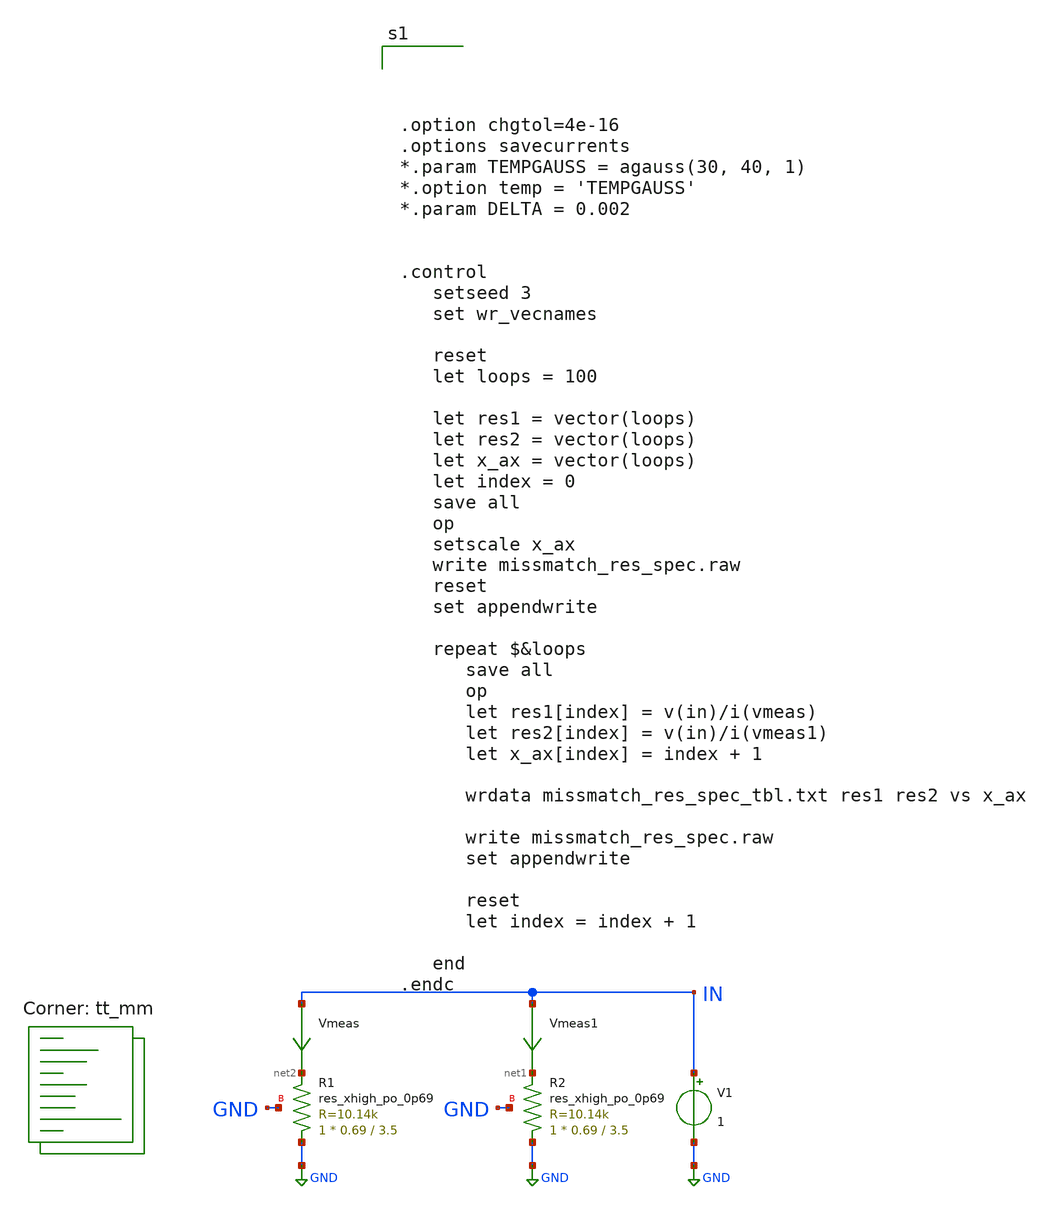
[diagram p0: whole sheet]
** sch_path: xschem/missmatch_res_spec.sch
**.subckt missmatch_res_spec
V1 IN GND 1
XR2 GND net1 GND sky130_fd_pr__res_xhigh_po_0p69 L=3.5 mult=1 m=1
XR1 GND net2 GND sky130_fd_pr__res_xhigh_po_0p69 L=3.5 mult=1 m=1
Vmeas IN net2 0
.save i(vmeas)
Vmeas1 IN net1 0
.save i(vmeas1)
**** begin user architecture code
.lib $::SKYWATER_MODELS/sky130.lib.spice tt_mm




.option chgtol=4e-16
.options savecurrents
*.param TEMPGAUSS = agauss(30, 40, 1)
*.option temp = 'TEMPGAUSS'
*.param DELTA = 0.002


.control
   setseed 3
   set wr_vecnames

   reset
   let loops = 100

   let res1 = vector(loops)
   let res2 = vector(loops)
   let x_ax = vector(loops)
   let index = 0
   save all
   op
   setscale x_ax
   write missmatch_res_spec.raw
   reset
   set appendwrite

   repeat $&loops
      save all
      op
      let res1[index] = v(in)/i(vmeas)
      let res2[index] = v(in)/i(vmeas1)
      let x_ax[index] = index + 1

      wrdata missmatch_res_spec_tbl.txt res1 res2 vs x_ax

      write missmatch_res_spec.raw
      set appendwrite

      reset
      let index = index + 1

   end
.endc


**** end user architecture code
**.ends
.GLOBAL GND
.end
